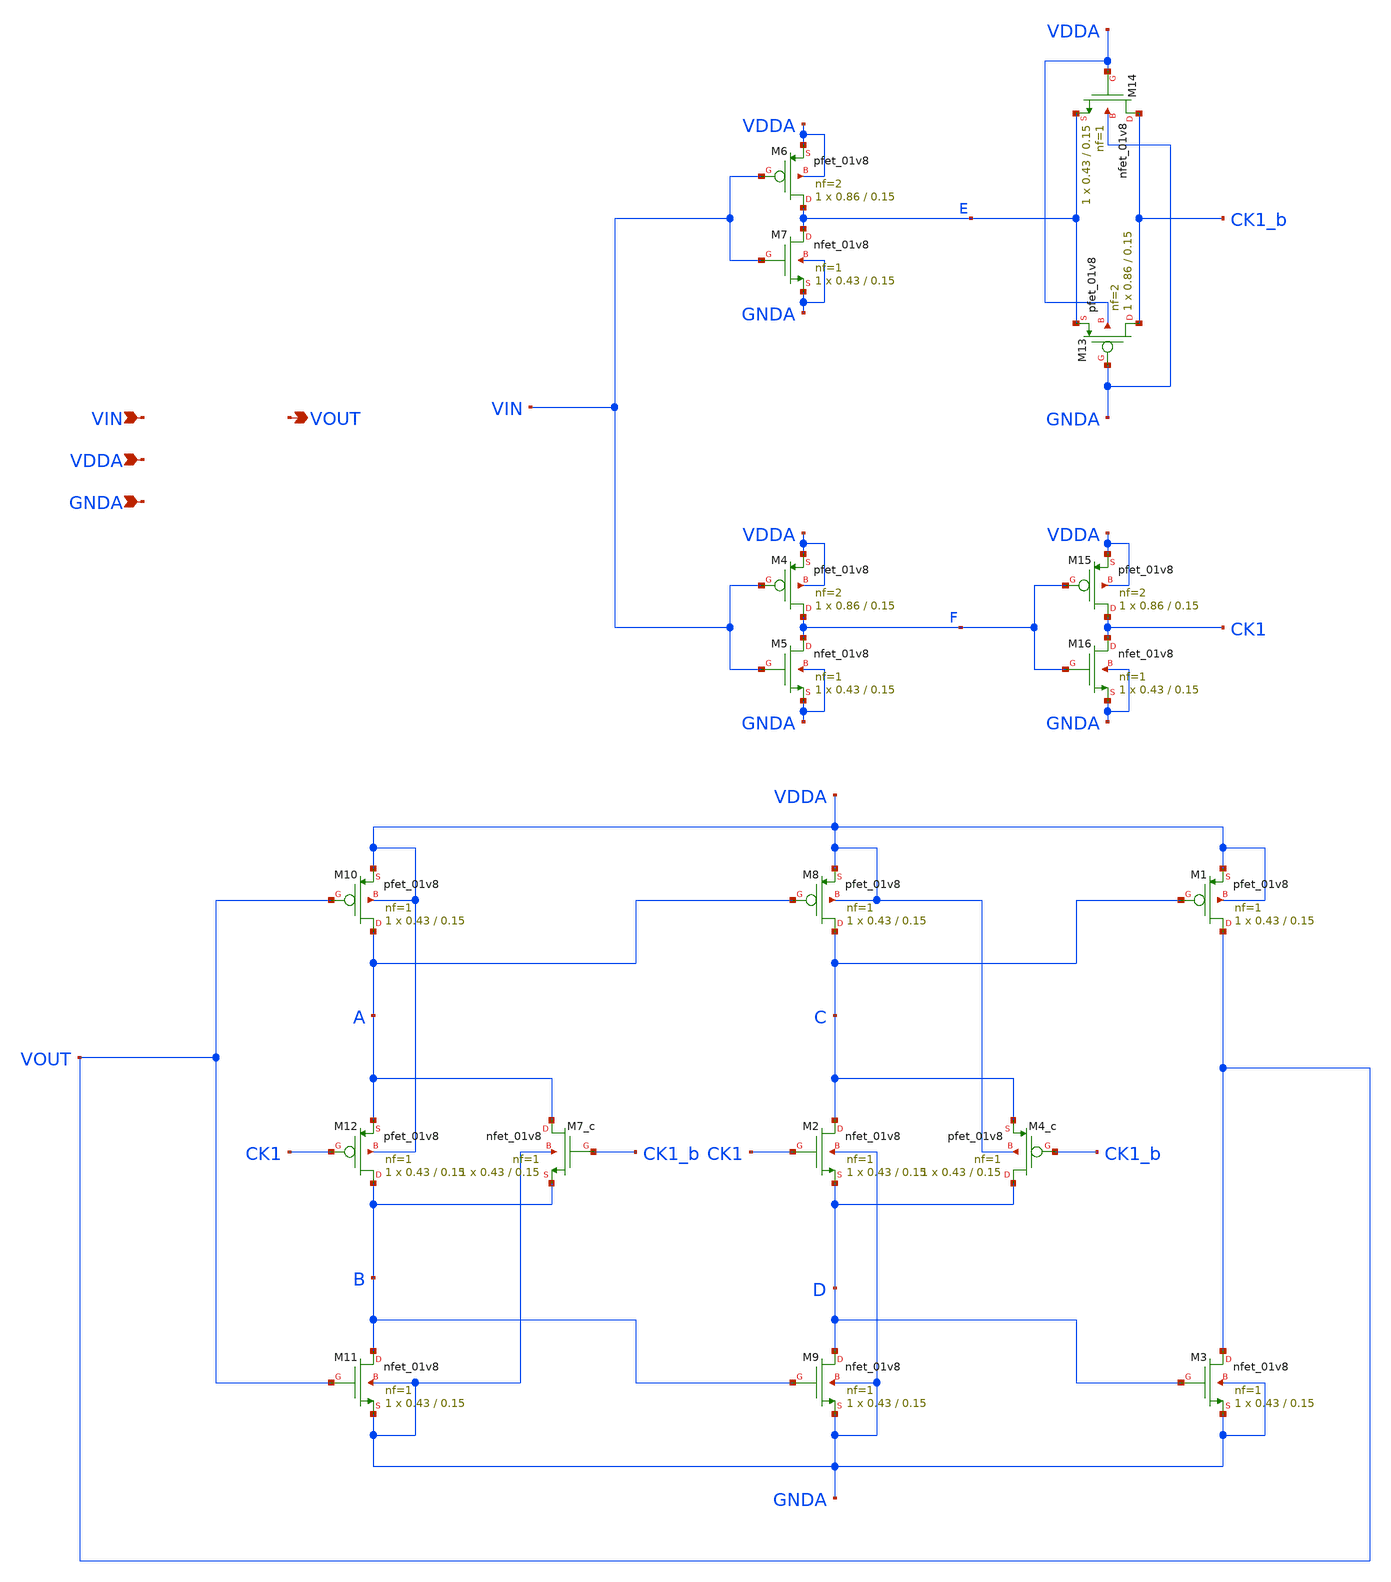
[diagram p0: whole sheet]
** sch_path: projects/pll/divider/xschem_ngspice/FF_comp_sw_divide2_2.sch
**.subckt FF_comp_sw_divide2_2 VIN VOUT VDDA GNDA
*.ipin VIN
*.opin VOUT
*.ipin VDDA
*.ipin GNDA
XM1 VOUT C VDDA VDDA sky130_fd_pr__pfet_01v8 L=0.15 W=0.43 nf=1 ad='int((nf+1)/2) * W/nf * 0.29' as='int((nf+2)/2) * W/nf * 0.29'
+ pd='2*int((nf+1)/2) * (W/nf + 0.29)' ps='2*int((nf+2)/2) * (W/nf + 0.29)' nrd='0.29 / W' nrs='0.29 / W'
+ sa=0 sb=0 sd=0 mult=1 m=1
XM2 C CK1 D GNDA sky130_fd_pr__nfet_01v8 L=0.15 W=0.43 nf=1 ad='int((nf+1)/2) * W/nf * 0.29' as='int((nf+2)/2) * W/nf * 0.29'
+ pd='2*int((nf+1)/2) * (W/nf + 0.29)' ps='2*int((nf+2)/2) * (W/nf + 0.29)' nrd='0.29 / W' nrs='0.29 / W'
+ sa=0 sb=0 sd=0 mult=1 m=1
XM3 VOUT D GNDA GNDA sky130_fd_pr__nfet_01v8 L=0.15 W=0.43 nf=1 ad='int((nf+1)/2) * W/nf * 0.29' as='int((nf+2)/2) * W/nf * 0.29'
+ pd='2*int((nf+1)/2) * (W/nf + 0.29)' ps='2*int((nf+2)/2) * (W/nf + 0.29)' nrd='0.29 / W' nrs='0.29 / W'
+ sa=0 sb=0 sd=0 mult=1 m=1
XM8 C A VDDA VDDA sky130_fd_pr__pfet_01v8 L=0.15 W=0.43 nf=1 ad='int((nf+1)/2) * W/nf * 0.29' as='int((nf+2)/2) * W/nf * 0.29'
+ pd='2*int((nf+1)/2) * (W/nf + 0.29)' ps='2*int((nf+2)/2) * (W/nf + 0.29)' nrd='0.29 / W' nrs='0.29 / W'
+ sa=0 sb=0 sd=0 mult=1 m=1
XM9 D B GNDA GNDA sky130_fd_pr__nfet_01v8 L=0.15 W=0.43 nf=1 ad='int((nf+1)/2) * W/nf * 0.29' as='int((nf+2)/2) * W/nf * 0.29'
+ pd='2*int((nf+1)/2) * (W/nf + 0.29)' ps='2*int((nf+2)/2) * (W/nf + 0.29)' nrd='0.29 / W' nrs='0.29 / W'
+ sa=0 sb=0 sd=0 mult=1 m=1
XM10 A VOUT VDDA VDDA sky130_fd_pr__pfet_01v8 L=0.15 W=0.43 nf=1 ad='int((nf+1)/2) * W/nf * 0.29' as='int((nf+2)/2) * W/nf * 0.29'
+ pd='2*int((nf+1)/2) * (W/nf + 0.29)' ps='2*int((nf+2)/2) * (W/nf + 0.29)' nrd='0.29 / W' nrs='0.29 / W'
+ sa=0 sb=0 sd=0 mult=1 m=1
XM11 B VOUT GNDA GNDA sky130_fd_pr__nfet_01v8 L=0.15 W=0.43 nf=1 ad='int((nf+1)/2) * W/nf * 0.29' as='int((nf+2)/2) * W/nf * 0.29'
+ pd='2*int((nf+1)/2) * (W/nf + 0.29)' ps='2*int((nf+2)/2) * (W/nf + 0.29)' nrd='0.29 / W' nrs='0.29 / W'
+ sa=0 sb=0 sd=0 mult=1 m=1
XM12 B CK1 A VDDA sky130_fd_pr__pfet_01v8 L=0.15 W=0.43 nf=1 ad='int((nf+1)/2) * W/nf * 0.29' as='int((nf+2)/2) * W/nf * 0.29'
+ pd='2*int((nf+1)/2) * (W/nf + 0.29)' ps='2*int((nf+2)/2) * (W/nf + 0.29)' nrd='0.29 / W' nrs='0.29 / W'
+ sa=0 sb=0 sd=0 mult=1 m=1
XM4_c D CK1_b C VDDA sky130_fd_pr__pfet_01v8 L=0.15 W=0.43 nf=1 ad='int((nf+1)/2) * W/nf * 0.29' as='int((nf+2)/2) * W/nf * 0.29'
+ pd='2*int((nf+1)/2) * (W/nf + 0.29)' ps='2*int((nf+2)/2) * (W/nf + 0.29)' nrd='0.29 / W' nrs='0.29 / W'
+ sa=0 sb=0 sd=0 mult=1 m=1
XM7_c A CK1_b B GNDA sky130_fd_pr__nfet_01v8 L=0.15 W=0.43 nf=1 ad='int((nf+1)/2) * W/nf * 0.29' as='int((nf+2)/2) * W/nf * 0.29'
+ pd='2*int((nf+1)/2) * (W/nf + 0.29)' ps='2*int((nf+2)/2) * (W/nf + 0.29)' nrd='0.29 / W' nrs='0.29 / W'
+ sa=0 sb=0 sd=0 mult=1 m=1
XM13 CK1_b GNDA E VDDA sky130_fd_pr__pfet_01v8 L=0.15 W=0.86 nf=2 ad='int((nf+1)/2) * W/nf * 0.29' as='int((nf+2)/2) * W/nf * 0.29'
+ pd='2*int((nf+1)/2) * (W/nf + 0.29)' ps='2*int((nf+2)/2) * (W/nf + 0.29)' nrd='0.29 / W' nrs='0.29 / W'
+ sa=0 sb=0 sd=0 mult=1 m=1
XM14 CK1_b VDDA E GNDA sky130_fd_pr__nfet_01v8 L=0.15 W=0.43 nf=1 ad='int((nf+1)/2) * W/nf * 0.29' as='int((nf+2)/2) * W/nf * 0.29'
+ pd='2*int((nf+1)/2) * (W/nf + 0.29)' ps='2*int((nf+2)/2) * (W/nf + 0.29)' nrd='0.29 / W' nrs='0.29 / W'
+ sa=0 sb=0 sd=0 mult=1 m=1
XM15 CK1 F VDDA VDDA sky130_fd_pr__pfet_01v8 L=0.15 W=0.86 nf=2 ad='int((nf+1)/2) * W/nf * 0.29' as='int((nf+2)/2) * W/nf * 0.29'
+ pd='2*int((nf+1)/2) * (W/nf + 0.29)' ps='2*int((nf+2)/2) * (W/nf + 0.29)' nrd='0.29 / W' nrs='0.29 / W'
+ sa=0 sb=0 sd=0 mult=1 m=1
XM16 CK1 F GNDA GNDA sky130_fd_pr__nfet_01v8 L=0.15 W=0.43 nf=1 ad='int((nf+1)/2) * W/nf * 0.29' as='int((nf+2)/2) * W/nf * 0.29'
+ pd='2*int((nf+1)/2) * (W/nf + 0.29)' ps='2*int((nf+2)/2) * (W/nf + 0.29)' nrd='0.29 / W' nrs='0.29 / W'
+ sa=0 sb=0 sd=0 mult=1 m=1
XM4 F VIN VDDA VDDA sky130_fd_pr__pfet_01v8 L=0.15 W=0.86 nf=2 ad='int((nf+1)/2) * W/nf * 0.29' as='int((nf+2)/2) * W/nf * 0.29'
+ pd='2*int((nf+1)/2) * (W/nf + 0.29)' ps='2*int((nf+2)/2) * (W/nf + 0.29)' nrd='0.29 / W' nrs='0.29 / W'
+ sa=0 sb=0 sd=0 mult=1 m=1
XM5 F VIN GNDA GNDA sky130_fd_pr__nfet_01v8 L=0.15 W=0.43 nf=1 ad='int((nf+1)/2) * W/nf * 0.29' as='int((nf+2)/2) * W/nf * 0.29'
+ pd='2*int((nf+1)/2) * (W/nf + 0.29)' ps='2*int((nf+2)/2) * (W/nf + 0.29)' nrd='0.29 / W' nrs='0.29 / W'
+ sa=0 sb=0 sd=0 mult=1 m=1
XM6 E VIN VDDA VDDA sky130_fd_pr__pfet_01v8 L=0.15 W=0.86 nf=2 ad='int((nf+1)/2) * W/nf * 0.29' as='int((nf+2)/2) * W/nf * 0.29'
+ pd='2*int((nf+1)/2) * (W/nf + 0.29)' ps='2*int((nf+2)/2) * (W/nf + 0.29)' nrd='0.29 / W' nrs='0.29 / W'
+ sa=0 sb=0 sd=0 mult=1 m=1
XM7 E VIN GNDA GNDA sky130_fd_pr__nfet_01v8 L=0.15 W=0.43 nf=1 ad='int((nf+1)/2) * W/nf * 0.29' as='int((nf+2)/2) * W/nf * 0.29'
+ pd='2*int((nf+1)/2) * (W/nf + 0.29)' ps='2*int((nf+2)/2) * (W/nf + 0.29)' nrd='0.29 / W' nrs='0.29 / W'
+ sa=0 sb=0 sd=0 mult=1 m=1
**.ends
.end
